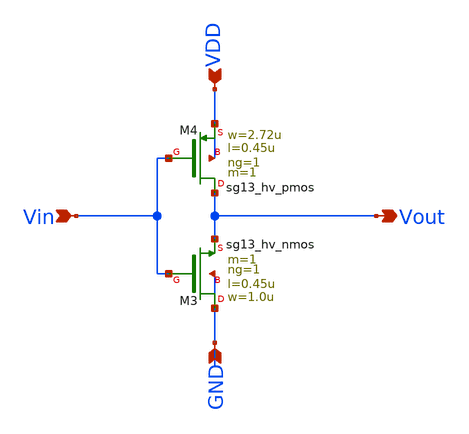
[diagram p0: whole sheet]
** sch_path: xschem/LogicGates/NOT.sch
**.subckt NOT VDD Vin GND Vout
*.ipin VDD
*.ipin Vin
*.ipin GND
*.opin Vout
XM3 GND Vin Vout GND sg13_hv_nmos w=1.0u l=0.45u ng=1 m=1 mm_ok=1
XM4 Vout Vin VDD VDD sg13_hv_pmos w=2.72u l=0.45u ng=1 m=1 mm_ok=1
**.ends
.end
